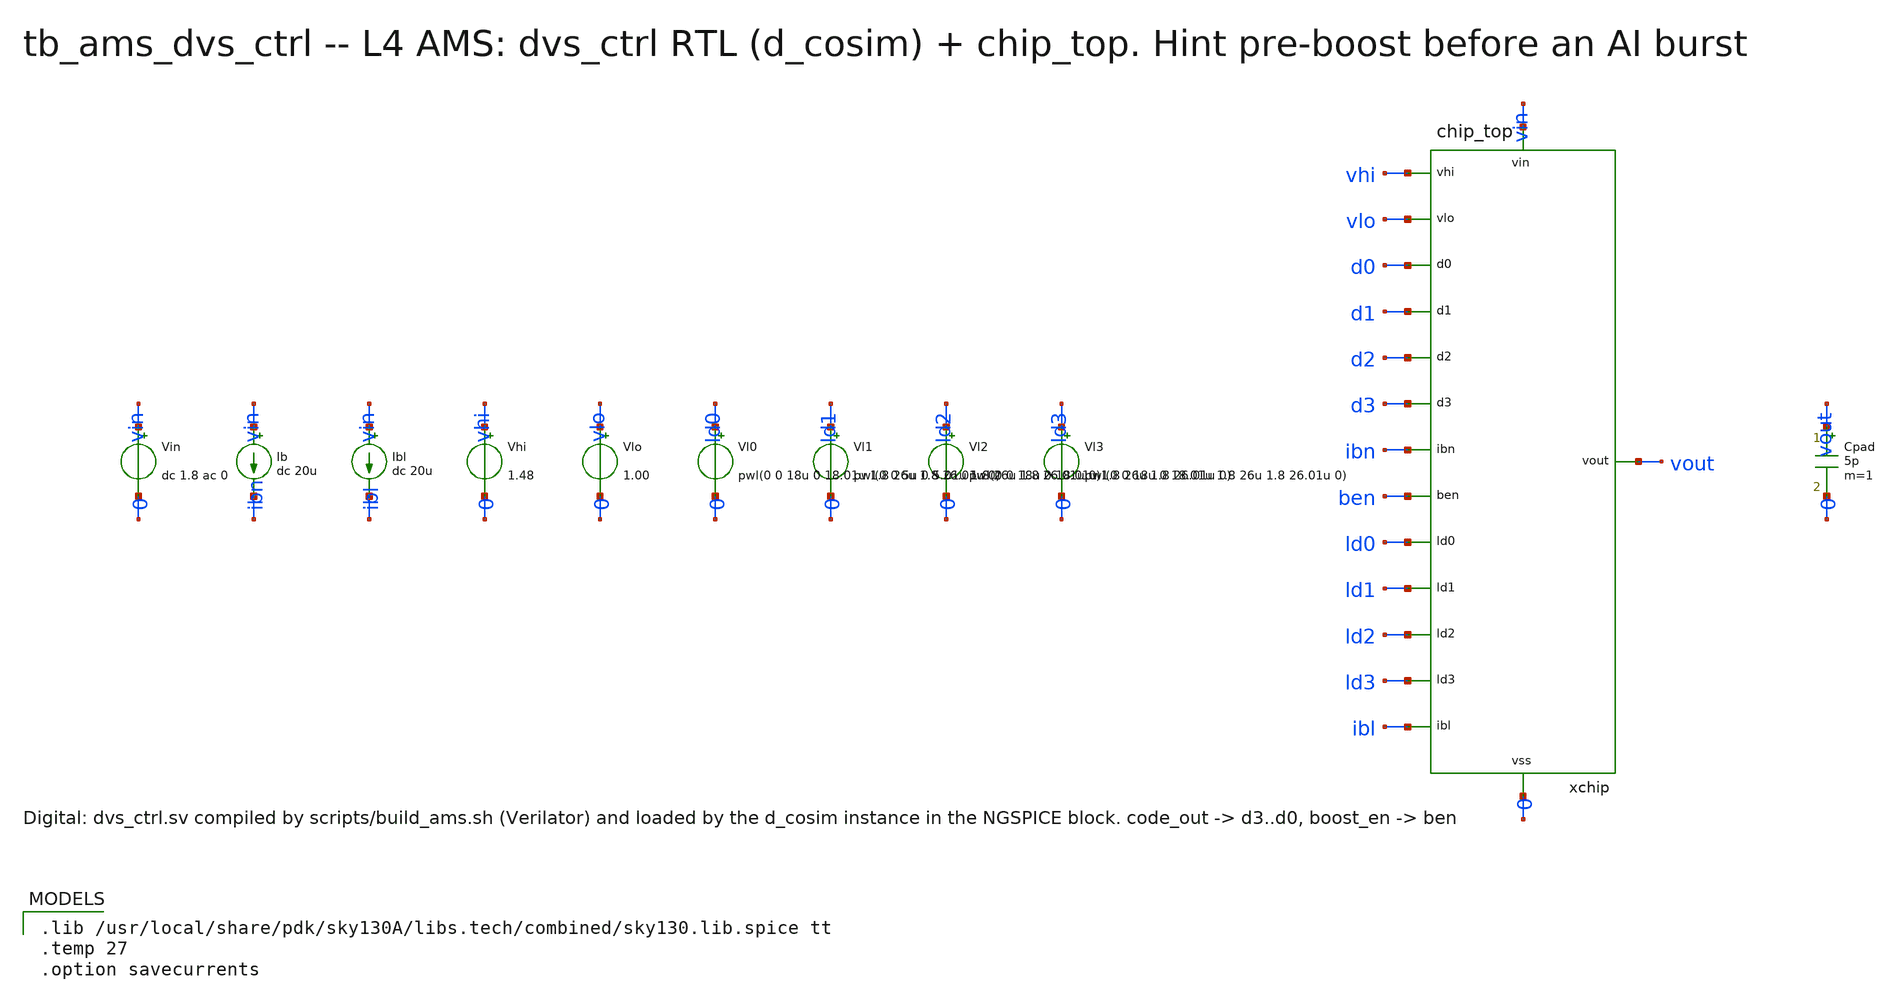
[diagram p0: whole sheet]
** sch_path: xschem/onetops_tb/tb_ams_dvs_ctrl.sch
**.subckt tb_ams_dvs_ctrl
Vin vin 0 dc 1.8 ac 0
Ib vin ibn dc 20u
Ibl vin ibl dc 20u
Vhi vhi 0 1.48
Vlo vlo 0 1.00
Vl0 ld0 0 pwl(0 0 18u 0 18.01u 1.8 26u 1.8 26.01u 0)
Vl1 ld1 0 pwl(0 0 5u 0 5.01u 1.8 26u 1.8 26.01u 0)
Vl2 ld2 0 pwl(0 0 18u 0 18.01u 1.8 26u 1.8 26.01u 0)
Vl3 ld3 0 pwl(0 0 18u 0 18.01u 1.8 26u 1.8 26.01u 0)
xchip vhi vlo d0 d1 d2 d3 ibn ben ld0 ld1 ld2 ld3 ibl vout vin 0 chip_top
Cpad vout 0 5p m=1
**** begin user architecture code

.lib /usr/local/share/pdk/sky130A/libs.tech/combined/sky130.lib.spice tt
.temp 27
.option savecurrents


* ---- digital side (XSPICE). Stimulus: analog PWL -> adc_bridge
Vclk aclk 0 pulse(0 1.8 0 1n 1n 49n 100n)
Vrst arst 0 pwl(0 0 1u 0 1.001u 1.8)
* code_req = 7 (0111) until 30 us, then 4 (0100)
Vcr3 acr3 0 dc 0
Vcr2 acr2 0 dc 1.8
Vcr1 acr1 0 pwl(0 1.8 30u 1.8 30.001u 0)
Vcr0 acr0 0 pwl(0 1.8 30u 1.8 30.001u 0)
* workload hint: AI burst expected -> raise VOUT 3 codes and enable boost (12 us .. 28 us)
Vhint ahint 0 pwl(0 0 12u 0 12.001u 1.8 28u 1.8 28.001u 0)
abrin [aclk arst acr3 acr2 acr1 acr0 ahint] [dclk drst dcr3 dcr2 dcr1 dcr0 dhint] adcb
.model adcb adc_bridge in_low=0.9 in_high=0.9
* port order = Verilog port order, vectors MSB first
adut [dclk drst dcr3 dcr2 dcr1 dcr0 dhint] [dco3 dco2 dco1 dco0 dben dset] dvs
.model dvs d_cosim simulation=../ams/dvs_ctrl.so
abrout [dco3 dco2 dco1 dco0 dben dset] [d3 d2 d1 d0 ben settled] dacb
.model dacb dac_bridge out_low=0 out_high=1.8 t_rise=2n t_fall=2n
.control
tran 5n 45u 0 1n
let code = (v(d0) + 2*v(d1) + 4*v(d2) + 8*v(d3))/1.8
meas tran code_a find code at=11.5u
meas tran vout_a find v(vout) at=11.5u
meas tran code_b find code at=17.5u
meas tran vout_b find v(vout) at=17.5u
meas tran vmin_burst min v(vout) from=18u to=20u
meas tran code_c find code at=44u
meas tran vout_c find v(vout) at=44u
let dip_mV = (vout_b - vmin_burst)*1000
echo AMS req7: code=$&code_a vout=$&vout_a
echo AMS hint: code=$&code_b vout=$&vout_b  burst dip_mV=$&dip_mV
echo AMS req4: code=$&code_c vout=$&vout_c
write tb_ams_dvs_ctrl.raw v(vout) v(xchip.xldo.vref) code v(ben) v(settled) v(ld0)
if $?batchmode
else
plot v(vout) v(xchip.xldo.vref) title 'AMS: VOUT and VREF'
plot code title 'dvs_ctrl code_out'
plot v(ben) v(settled)+2 v(ld0)+4 title 'boost_en / settled / load'
end
.endc

**** end user architecture code
**.ends
.end
